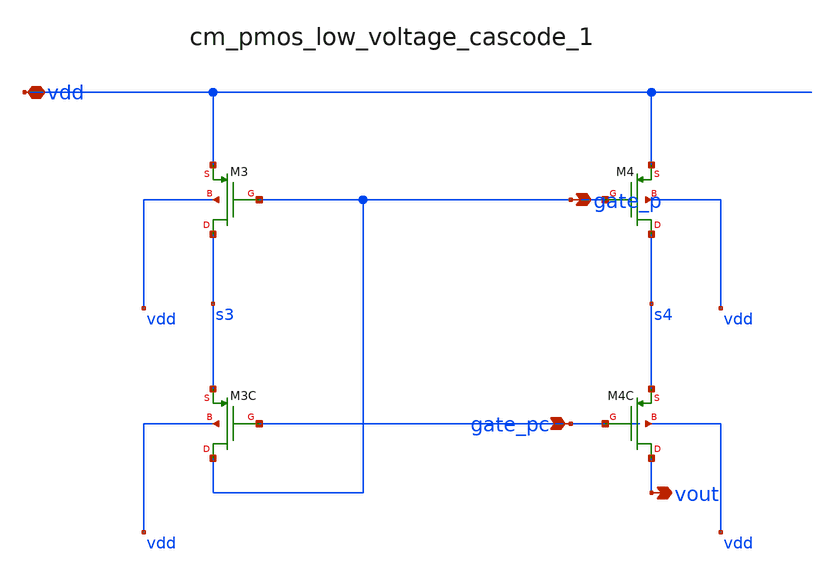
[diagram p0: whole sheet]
** sch_path: analog-db/raw/amp_018_telescopic_cascode/hier/blocks/cm_pmos_low_voltage_cascode_1.sch
**.subckt cm_pmos_low_voltage_cascode_1 gate_pc vdd gate_p vout
*.ipin gate_pc
*.iopin vdd
*.opin gate_p
*.opin vout
XM3 s3 gate_p vdd vdd sg13_lv_pmos w=x_dut_xm3_w l=x_dut_xm3_l ng=1 m=x_dut_xm3_m
XM3C gate_p gate_pc s3 vdd sg13_lv_pmos w=x_dut_xm3c_w l=x_dut_xm3c_l ng=1 m=x_dut_xm3c_m
XM4 s4 gate_p vdd vdd sg13_lv_pmos w=x_dut_xm4_w l=x_dut_xm4_l ng=1 m=x_dut_xm4_m
XM4C vout gate_pc s4 vdd sg13_lv_pmos w=x_dut_xm4c_w l=x_dut_xm4c_l ng=1 m=x_dut_xm4c_m
**.ends
.end
